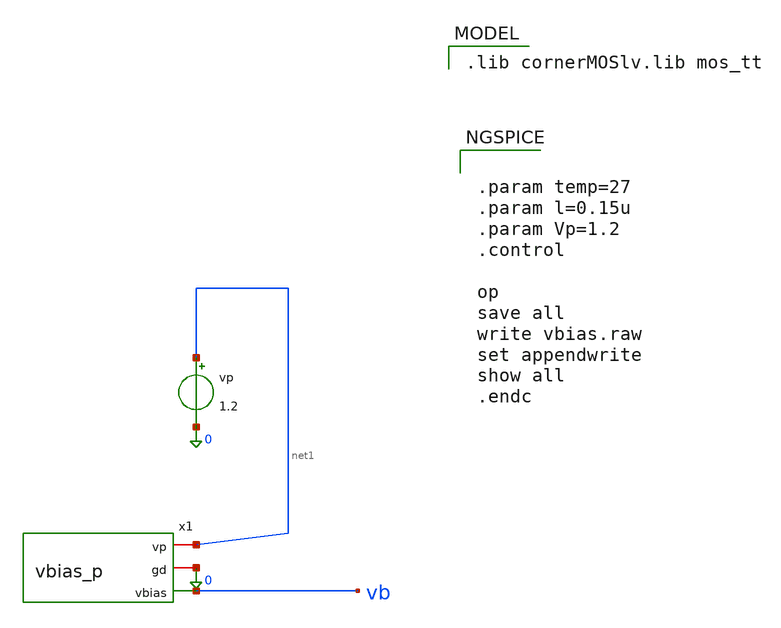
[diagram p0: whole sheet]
** sch_path: charge_pump/vbias_tb.sch
**.subckt vbias_tb
vp net1 0 1.2
x1 net1 0 vb vbias_p
**** begin user architecture code
 .lib cornerMOSlv.lib mos_tt



.param temp=27
.param l=0.15u
.param Vp=1.2
.control

op
save all
write vbias.raw
set appendwrite
show all
.endc


**** end user architecture code
**.ends

* expanding   symbol:  /foss/designs/CHIP-PLL/charge_pump/vbias_p.sym # of pins=3
** sym_path: charge_pump/vbias_p.sym
** sch_path: charge_pump/vbias_p.sch
.subckt vbias_p vp gd vbias
*.iopin vp
*.iopin gd
*.opin vbias
XM16 net2 net2 0 gd sg13_lv_nmos w=1.6u l=0.6u ng=1 m=1 mm_ok=1
XM1 vbias net1 net2 gd sg13_lv_nmos w=1.6u l=0.6u ng=1 m=1 mm_ok=1
R1 net1 vbias 500 m=1
XM5 iref iref vp vp sg13_lv_pmos w=1.4u l=0.6u ng=1 m=1 mm_ok=1
XM6 net3 iref vp vp sg13_lv_pmos w=1u l=0.6u ng=1 m=1 mm_ok=1
XM7 iref net3 net4 gd sg13_lv_nmos w=1u l=0.6u ng=1 m=1 mm_ok=1
XM8 net3 net3 gd gd sg13_lv_nmos w=1.4u l=0.6u ng=1 m=1 mm_ok=1
R3 net4 gd 500 m=1
XM10 net1 iref vp vp sg13_lv_pmos w=1.6u l=0.6u ng=1 m=1 mm_ok=1
.ends

.end
